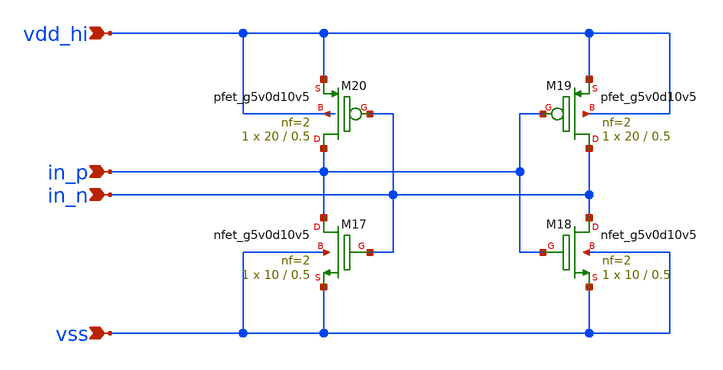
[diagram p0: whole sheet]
** sch_path: xschem/audiodac_drv_latch.sch
* (c) 2022 Harald Pretl, IIC, Johannes Kepler University
**.subckt audiodac_drv_latch in_p in_n vdd_hi vss
*.ipin in_p
*.ipin in_n
*.ipin vdd_hi
*.ipin vss
XM19 in_n in_p vdd_hi vdd_hi sky130_fd_pr__pfet_g5v0d10v5 L=0.5 W=20 nf=2 ad='int((2 + 1)/2) * 20 / 2 * 0.29'
+ as='int((2 + 2)/2) * 20 / 2 * 0.29' pd='2*int((2 + 1)/2) * (20 / 2 + 0.29)' ps='2*int((2 + 2)/2) * (20 / 2 + 0.29)'
+ nrd='0.29 / 20 ' nrs='0.29 / 20 ' sa=0 sb=0 sd=0 mult=1 m=1
XM18 in_n in_p vss vss sky130_fd_pr__nfet_g5v0d10v5 L=0.5 W=10 nf=2 ad='int((2 + 1)/2) * 10 / 2 * 0.29'
+ as='int((2 + 2)/2) * 10 / 2 * 0.29' pd='2*int((2 + 1)/2) * (10 / 2 + 0.29)' ps='2*int((2 + 2)/2) * (10 / 2 + 0.29)'
+ nrd='0.29 / 10 ' nrs='0.29 / 10 ' sa=0 sb=0 sd=0 mult=1 m=1
XM20 in_p in_n vdd_hi vdd_hi sky130_fd_pr__pfet_g5v0d10v5 L=0.5 W=20 nf=2 ad='int((2 + 1)/2) * 20 / 2 * 0.29'
+ as='int((2 + 2)/2) * 20 / 2 * 0.29' pd='2*int((2 + 1)/2) * (20 / 2 + 0.29)' ps='2*int((2 + 2)/2) * (20 / 2 + 0.29)'
+ nrd='0.29 / 20 ' nrs='0.29 / 20 ' sa=0 sb=0 sd=0 mult=1 m=1
XM17 in_p in_n vss vss sky130_fd_pr__nfet_g5v0d10v5 L=0.5 W=10 nf=2 ad='int((2 + 1)/2) * 10 / 2 * 0.29'
+ as='int((2 + 2)/2) * 10 / 2 * 0.29' pd='2*int((2 + 1)/2) * (10 / 2 + 0.29)' ps='2*int((2 + 2)/2) * (10 / 2 + 0.29)'
+ nrd='0.29 / 10 ' nrs='0.29 / 10 ' sa=0 sb=0 sd=0 mult=1 m=1
**.ends
.end
